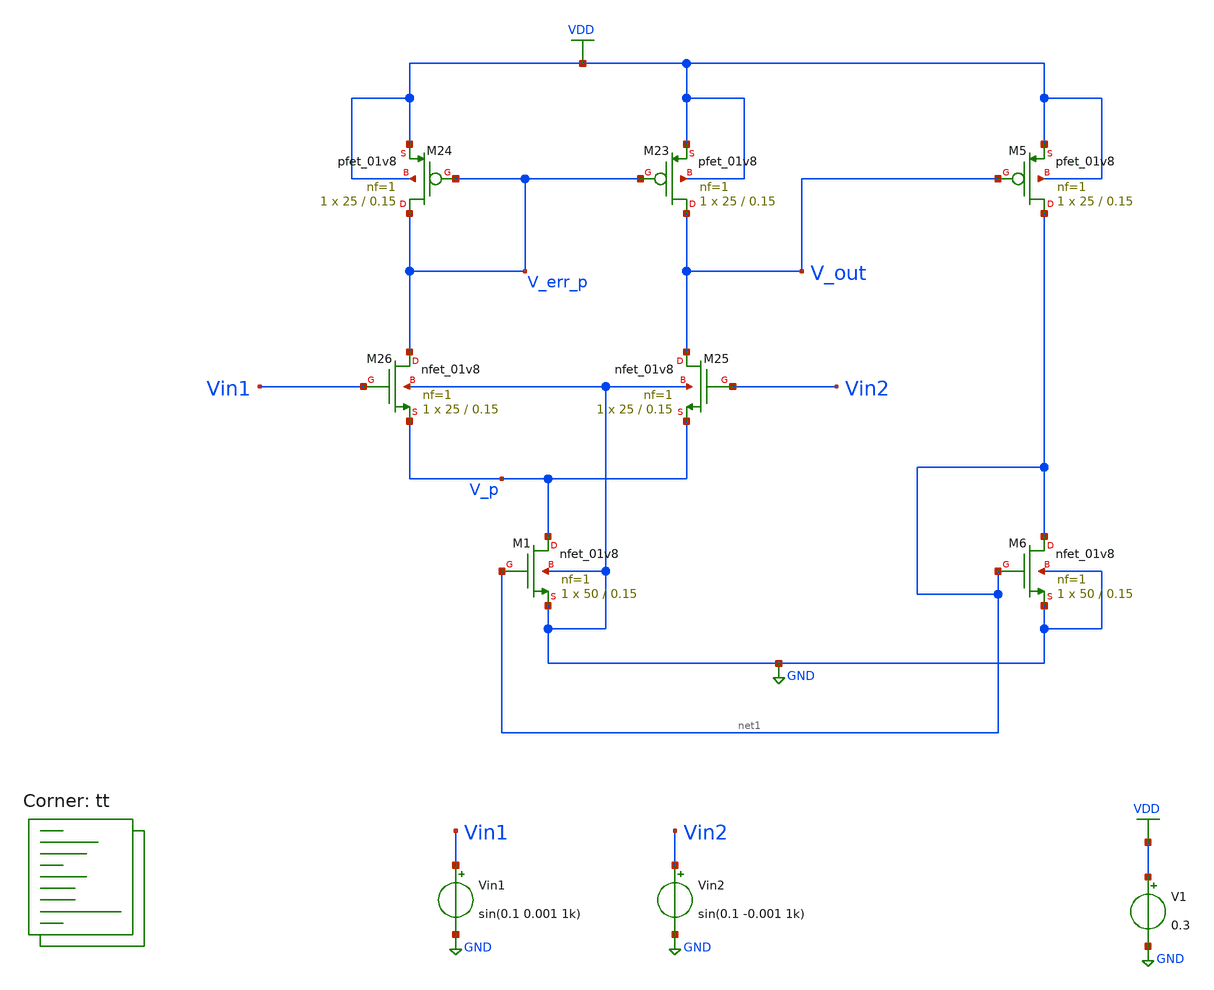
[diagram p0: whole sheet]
** sch_path: projects/bandgapref/xschem_ngspice/new_files/tb_opamp_bandgap_2.sch
**.subckt tb_opamp_bandgap_2
V1 VDD GND 0.3
Vin1 Vin1 GND sin(0.1 0.001 1k)
Vin2 Vin2 GND sin(0.1 -0.001 1k)
XM23 V_out V_err_p VDD VDD sky130_fd_pr__pfet_01v8 L=0.15 W=25 nf=1 ad='int((nf+1)/2) * W/nf * 0.29'
+ as='int((nf+2)/2) * W/nf * 0.29' pd='2*int((nf+1)/2) * (W/nf + 0.29)' ps='2*int((nf+2)/2) * (W/nf + 0.29)'
+ nrd='0.29 / W' nrs='0.29 / W' sa=0 sb=0 sd=0 mult=1 m=1
XM24 V_err_p V_err_p VDD VDD sky130_fd_pr__pfet_01v8 L=0.15 W=25 nf=1 ad='int((nf+1)/2) * W/nf * 0.29'
+ as='int((nf+2)/2) * W/nf * 0.29' pd='2*int((nf+1)/2) * (W/nf + 0.29)' ps='2*int((nf+2)/2) * (W/nf + 0.29)'
+ nrd='0.29 / W' nrs='0.29 / W' sa=0 sb=0 sd=0 mult=1 m=1
XM25 V_out Vin2 V_p GND sky130_fd_pr__nfet_01v8 L=0.15 W=25 nf=1 ad='int((nf+1)/2) * W/nf * 0.29' as='int((nf+2)/2) * W/nf * 0.29'
+ pd='2*int((nf+1)/2) * (W/nf + 0.29)' ps='2*int((nf+2)/2) * (W/nf + 0.29)' nrd='0.29 / W' nrs='0.29 / W'
+ sa=0 sb=0 sd=0 mult=1 m=1
XM26 V_err_p Vin1 V_p GND sky130_fd_pr__nfet_01v8 L=0.15 W=25 nf=1 ad='int((nf+1)/2) * W/nf * 0.29' as='int((nf+2)/2) * W/nf * 0.29'
+ pd='2*int((nf+1)/2) * (W/nf + 0.29)' ps='2*int((nf+2)/2) * (W/nf + 0.29)' nrd='0.29 / W' nrs='0.29 / W'
+ sa=0 sb=0 sd=0 mult=1 m=1
XM1 V_p net1 GND GND sky130_fd_pr__nfet_01v8 L=0.15 W=50 nf=1 ad='int((nf+1)/2) * W/nf * 0.29' as='int((nf+2)/2) * W/nf * 0.29'
+ pd='2*int((nf+1)/2) * (W/nf + 0.29)' ps='2*int((nf+2)/2) * (W/nf + 0.29)' nrd='0.29 / W' nrs='0.29 / W'
+ sa=0 sb=0 sd=0 mult=1 m=1
XM5 net1 V_out VDD VDD sky130_fd_pr__pfet_01v8 L=0.15 W=25 nf=1 ad='int((nf+1)/2) * W/nf * 0.29' as='int((nf+2)/2) * W/nf * 0.29'
+ pd='2*int((nf+1)/2) * (W/nf + 0.29)' ps='2*int((nf+2)/2) * (W/nf + 0.29)' nrd='0.29 / W' nrs='0.29 / W'
+ sa=0 sb=0 sd=0 mult=1 m=1
XM6 net1 net1 GND GND sky130_fd_pr__nfet_01v8 L=0.15 W=50 nf=1 ad='int((nf+1)/2) * W/nf * 0.29' as='int((nf+2)/2) * W/nf * 0.29'
+ pd='2*int((nf+1)/2) * (W/nf + 0.29)' ps='2*int((nf+2)/2) * (W/nf + 0.29)' nrd='0.29 / W' nrs='0.29 / W'
+ sa=0 sb=0 sd=0 mult=1 m=1
**** begin user architecture code



.option wnflag=1
.option savecurrents

.save @m.xm1.msky130_fd_pr__nfet_01v8[gm] @m.xm2.msky130_fd_pr__nfet_01v8[gm] @m.xm3.msky130_fd_pr__nfet_01v8[gm] @m.xm4.msky130_fd_pr__pfet_01v8[gm] @m.xm5.msky130_fd_pr__pfet_01v8[gm] @m.xm6.msky130_fd_pr__nfet_01v8[gm] @m.xm7.msky130_fd_pr__pfet_01v8[gm]

.control

  save all
   tran 1u 3m
   * ac dec 20 1 1T

  write tb_opamp_bandgap_2.raw
  set appendwrite

.endc



.lib $::SKYWATER_MODELS/sky130.lib.spice tt
**** end user architecture code
**.ends
.GLOBAL GND
.GLOBAL VDD
.end
